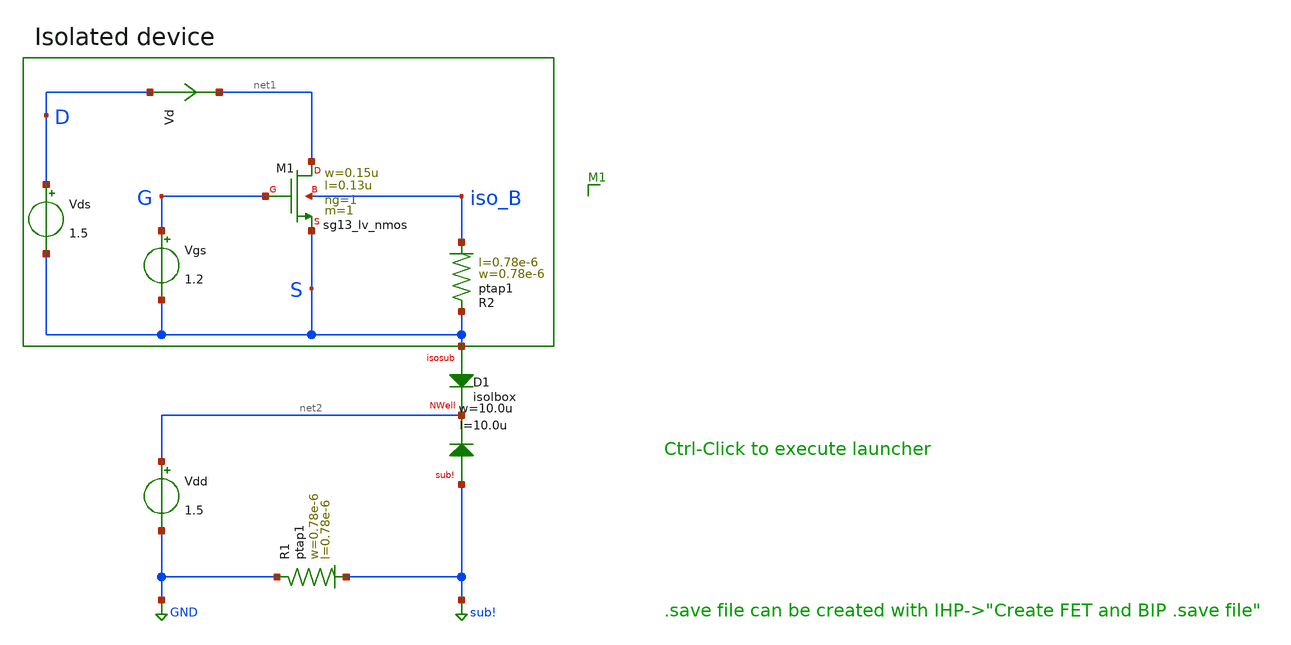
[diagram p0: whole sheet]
** sch_path: ihp-sg13g2/xschem_libs/sg13g2_tests_ase/iso_dc_lv_nmos/schematic/iso_dc_lv_nmos.sch
* Copyright 2023 IHP PDK Authors
**.subckt iso_dc_lv_nmos
Vgs G S 1.2
Vds D S 1.5
Vd D net1 0
.save i(vd)
XM1 net1 G S iso_B sg13_lv_nmos w=0.15u l=0.13u ng=1 m=1 mm_ok=1
XD1 S net2 sub! isolbox l=10.0u w=10.0u
XR1 GND sub! ptap1 R=262.8 w=0.78e-6 l=0.78e-6
XR2 S iso_B ptap1 R=262.8 w=0.78e-6 l=0.78e-6
Vdd net2 GND 1.5
**.ends
.GLOBAL GND
.GLOBAL sub!
.end
